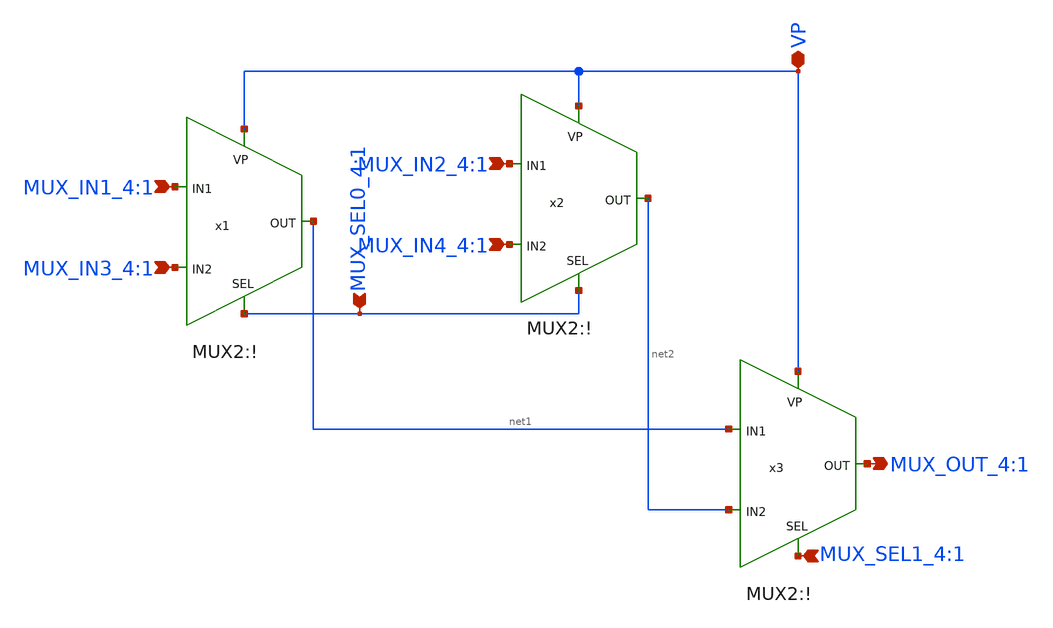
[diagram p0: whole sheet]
** sch_path: AllSymbols&Sch/MUX/MUX4:1.sch
**.subckt MUX4:1 MUX_SEL0_4:1 MUX_SEL1_4:1 MUX_IN1_4:1 MUX_IN3_4:1 MUX_IN2_4:1 MUX_IN4_4:1
*+ MUX_OUT_4:1 VP
*.ipin MUX_SEL0_4:1
*.ipin MUX_SEL1_4:1
*.ipin MUX_IN1_4:1
*.ipin MUX_IN3_4:1
*.ipin MUX_IN2_4:1
*.ipin MUX_IN4_4:1
*.opin MUX_OUT_4:1
*.iopin VP
x1 MUX_IN1_4:1 VP net1 MUX_IN3_4:1 MUX_SEL0_4:1 MUX2:!
x2 MUX_IN2_4:1 VP net2 MUX_IN4_4:1 MUX_SEL0_4:1 MUX2:!
x3 net1 VP MUX_OUT_4:1 net2 MUX_SEL1_4:1 MUX2:!
**.ends

* expanding   symbol:  /home/safal/projects/GitHub_CMOS_4bit_ALU/AllSymbols&Sch/MUX/MUX2:!.sym # of
*+ pins=5
** sym_path: AllSymbols&Sch/MUX/MUX2:!.sym
** sch_path: AllSymbols&Sch/MUX/MUX2:!.sch
.subckt MUX2:! MUX_IN1_2:1 VP MUX_OUT_2:1 MUX_IN2_2:1 MUX_SEL_2:1
*.ipin MUX_IN1_2:1
*.opin MUX_OUT_2:1
*.iopin VP
*.ipin MUX_IN2_2:1
*.ipin MUX_SEL_2:1
x1 MUX_SEL_2:1 VP MUX_IN1_2:1 MUX_OUT_2:1 net2 net1 TransmissionGate
x2 net1 VP MUX_IN2_2:1 MUX_OUT_2:1 net2 MUX_SEL_2:1 TransmissionGate
x3 VP net1 MUX_SEL_2:1 inverter
.ends


* expanding   symbol:
*+  /home/safal/projects/GitHub_CMOS_4bit_ALU/AllSymbols&Sch/GenericSym/TransmissionGate.sym # of pins=6
** sym_path: AllSymbols&Sch/GenericSym/TransmissionGate.sym
** sch_path: AllSymbols&Sch/GenericSym/TransmissionGate.sch
.subckt TransmissionGate X VP A Y VN X'
*.ipin A
*.opin Y
*.ipin X'
*.ipin X
*.iopin VP
*.iopin VN
XM1 A X Y VP sky130_fd_pr__pfet_01v8 L=0.15 W=1 nf=1 ad='int((1 + 1)/2) * 1 / 1 * 0.29' as='int((1 + 2)/2) * 1 / 1 * 0.29'
+ pd='2*int((1 + 1)/2) * (1 / 1 + 0.29)' ps='2*int((1 + 2)/2) * (1 / 1 + 0.29)' nrd='0.29 / 1 ' nrs='0.29 / 1 '
+ sa=0 sb=0 sd=0 mult=1 m=1
XM2 A X' Y VN sky130_fd_pr__nfet_01v8 L=0.15 W=1 nf=1 ad='int((1 + 1)/2) * 1 / 1 * 0.29' as='int((1 +
+ 2)/2) * 1 / 1 * 0.29' pd='2*int((1 + 1)/2) * (1 / 1 + 0.29)' ps='2*int((1 + 2)/2) * (1 / 1 + 0.29)' nrd='0.29
+ / 1 ' nrs='0.29 / 1 ' sa=0 sb=0 sd=0 mult=1 m=1
**** begin user architecture code

.lib /usr/local/share/pdk/sky130A/libs.tech/ngspice/sky130.lib.spice tt

**** end user architecture code
.ends


* expanding   symbol:  /home/safal/projects/GitHub_CMOS_4bit_ALU/AllSymbols&Sch/GenericSym/inverter.sym # of pins=3
** sym_path: AllSymbols&Sch/GenericSym/inverter.sym
** sch_path: AllSymbols&Sch/GenericSym/inverter.sch
.subckt inverter VP inv_out inv_in
*.ipin inv_in
*.opin inv_out
*.iopin VP
XM1 inv_out inv_in VP VP sky130_fd_pr__pfet_01v8 L=0.15 W=2 nf=1 ad='int((1 + 1)/2) * 2 / 1 * 0.29' as='int((1
+ + 2)/2) * 2 / 1 * 0.29' pd='2*int((1 + 1)/2) * (2 / 1 + 0.29)' ps='2*int((1 + 2)/2) * (2 / 1 + 0.29)' nrd='0.29
+ / 2 ' nrs='0.29 / 2 ' sa=0 sb=0 sd=0 mult=1 m=1
XM2 inv_out inv_in GND GND sky130_fd_pr__nfet_01v8 L=0.15 W=1 nf=1 ad='int((1 + 1)/2) * 1 / 1 * 0.29' as='int((1
+ + 2)/2) * 1 / 1 * 0.29' pd='2*int((1 + 1)/2) * (1 / 1 + 0.29)' ps='2*int((1 + 2)/2) * (1 / 1 + 0.29)' nrd='0.29
+ / 1 ' nrs='0.29 / 1 ' sa=0 sb=0 sd=0 mult=1 m=1
.ends

.GLOBAL GND
.end
